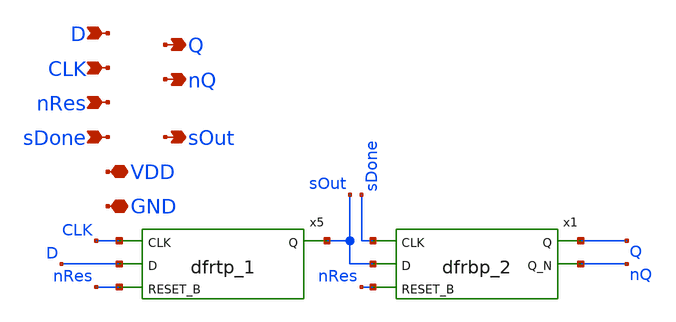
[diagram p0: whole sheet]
** sch_path: design/xschem/dflip_flop_std_fc.sch
**.subckt dflip_flop_std_fc D Q CLK nQ nRes sOut sDone VDD GND
*.ipin D
*.opin Q
*.ipin CLK
*.opin nQ
*.ipin nRes
*.opin sOut
*.ipin sDone
*.iopin VDD
*.iopin GND
x5 CLK D nRes GND GND VDD VDD sOut sky130_fd_sc_hd__dfrtp_1
x1 sDone sOut nRes GND GND VDD VDD Q nQ sky130_fd_sc_hd__dfrbp_2
**.ends
.end
